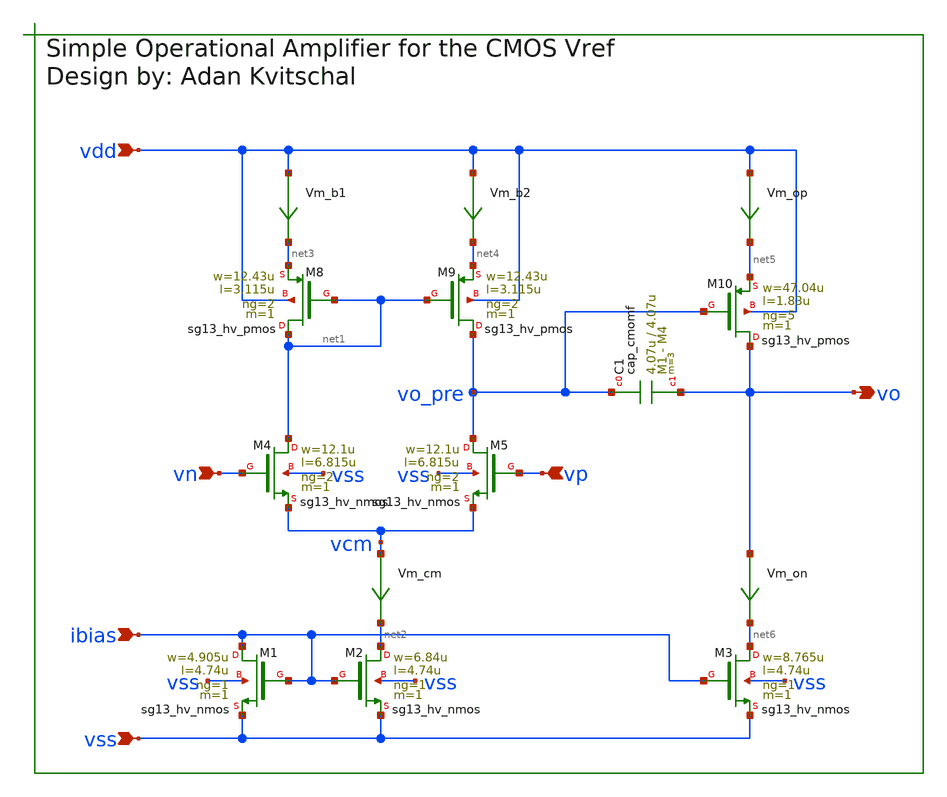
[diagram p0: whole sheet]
** sch_path: release/xschem/sch/output_amp.sch
**.subckt output_amp vp vn ibias vo vss vdd
*.ipin vp
*.ipin vn
*.ipin ibias
*.opin vo
*.ipin vss
*.ipin vdd
Vm_b1 vdd net3 0
.save i(vm_b1)
Vm_op vdd net5 0
.save i(vm_op)
Vm_cm vcm net2 0
.save i(vm_cm)
Vm_b2 vdd net4 0
.save i(vm_b2)
Vm_on vo net6 0
.save i(vm_on)
XM1 ibias ibias vss vss sg13_hv_nmos w=4.905u l=4.74u ng=1 m=1 mm_ok=1
XM2 net2 ibias vss vss sg13_hv_nmos w=6.84u l=4.74u ng=1 m=1 mm_ok=1
XM3 net6 ibias vss vss sg13_hv_nmos w=8.765u l=4.74u ng=1 m=1 mm_ok=1
XM4 net1 vn vcm vss sg13_hv_nmos w=12.1u l=6.815u ng=2 m=1 mm_ok=1
XM5 vo_pre vp vcm vss sg13_hv_nmos w=12.1u l=6.815u ng=2 m=1 mm_ok=1
XM8 net1 net1 net3 vdd sg13_hv_pmos w=12.43u l=3.115u ng=2 m=1 mm_ok=1
XM9 vo_pre net1 net4 vdd sg13_hv_pmos w=12.43u l=3.115u ng=2 m=1 mm_ok=1
XM10 vo vo_pre net5 vdd sg13_hv_pmos w=47.04u l=1.83u ng=5 m=1 mm_ok=1
XC1 vo_pre vo cap_cmomf w=4.07u l=4.07u mmin=1 mmax=4 subblock=0 rfmodel=0 subscale=1 m=3 mm_ok=1
**.ends
.end
